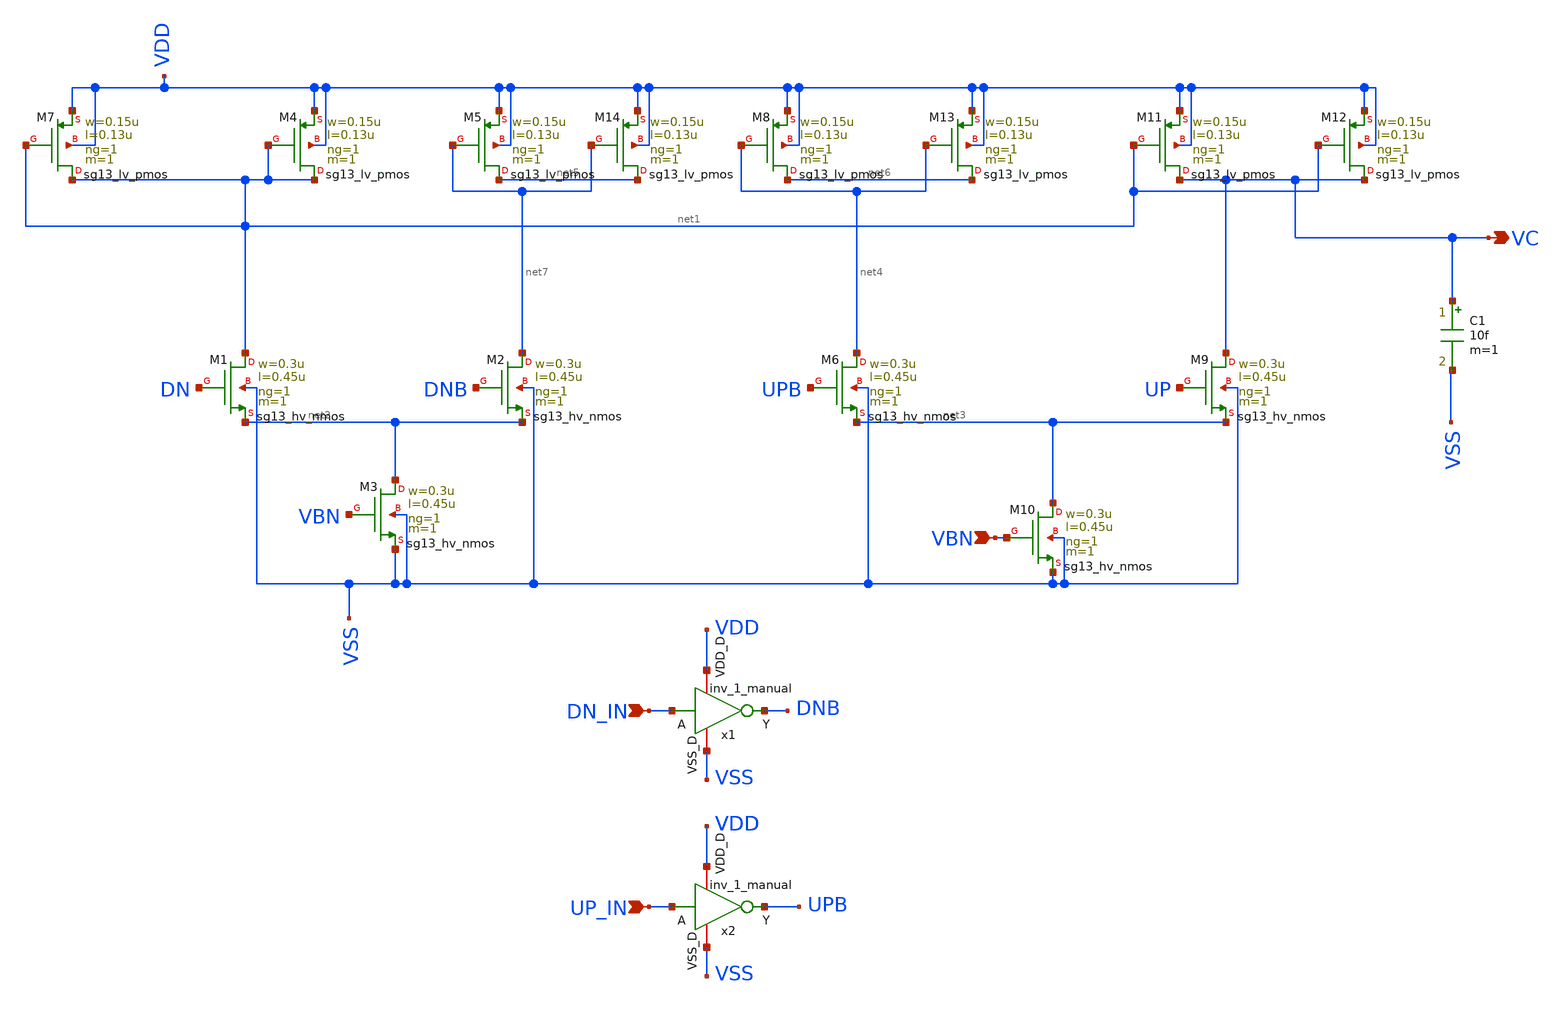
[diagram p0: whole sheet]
** sch_path: others/Charge-Pump.sch
**.subckt Charge-Pump VBN DN_IN UP_IN VC
*.ipin VBN
*.ipin DN_IN
*.ipin UP_IN
*.opin VC
XM1 net1 DN net2 VSS sg13_hv_nmos w=0.3u l=0.45u ng=1 m=1 mm_ok=1
XM7 net1 net1 VDD VDD sg13_lv_pmos w=0.15u l=0.13u ng=1 m=1 mm_ok=1
XM2 net7 DNB net2 VSS sg13_hv_nmos w=0.3u l=0.45u ng=1 m=1 mm_ok=1
XM3 net2 VBN VSS VSS sg13_hv_nmos w=0.3u l=0.45u ng=1 m=1 mm_ok=1
XM4 net1 net1 VDD VDD sg13_lv_pmos w=0.15u l=0.13u ng=1 m=1 mm_ok=1
XM5 net5 net7 VDD VDD sg13_lv_pmos w=0.15u l=0.13u ng=1 m=1 mm_ok=1
XM6 net4 UPB net3 VSS sg13_hv_nmos w=0.3u l=0.45u ng=1 m=1 mm_ok=1
XM8 net6 net4 VDD VDD sg13_lv_pmos w=0.15u l=0.13u ng=1 m=1 mm_ok=1
XM9 VC UP net3 VSS sg13_hv_nmos w=0.3u l=0.45u ng=1 m=1 mm_ok=1
XM10 net3 VBN VSS VSS sg13_hv_nmos w=0.3u l=0.45u ng=1 m=1 mm_ok=1
XM11 VC net1 VDD VDD sg13_lv_pmos w=0.15u l=0.13u ng=1 m=1 mm_ok=1
XM12 VC net1 VDD VDD sg13_lv_pmos w=0.15u l=0.13u ng=1 m=1 mm_ok=1
XM13 net6 net4 VDD VDD sg13_lv_pmos w=0.15u l=0.13u ng=1 m=1 mm_ok=1
XM14 net5 net7 VDD VDD sg13_lv_pmos w=0.15u l=0.13u ng=1 m=1 mm_ok=1
x1 VDD DN_IN DNB VSS inv_1_manual
x2 VDD UP_IN UPB VSS inv_1_manual
C1 VC net8 10f m=1
**.ends
.end
